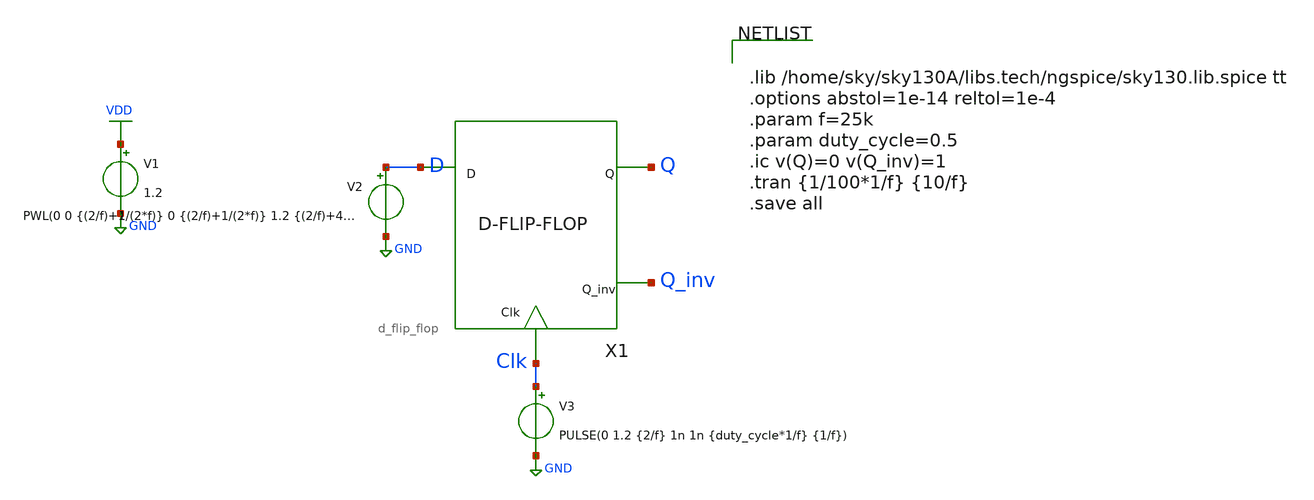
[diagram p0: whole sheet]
** sch_path: xschem/D_flip_flop/d_flip_flop_tb.sch
**.subckt d_flip_flop_tb
X1 D Q Q_inv Clk d_flip_flop
V1 VDD GND 1.2
V2 D GND PWL(0 0 {(2/f)+1/(2*f)} 0 {(2/f)+1/(2*f)} 1.2 {(2/f)+4/(2*f)} 1.2 {(2/f)+4/(2*f)} 0)
V3 Clk GND PULSE(0 1.2 {2/f} 1n 1n {duty_cycle*1/f} {1/f})
**** begin user architecture code


.lib /home/sky/sky130A/libs.tech/ngspice/sky130.lib.spice tt
.options abstol=1e-14 reltol=1e-4
.param f=25k
.param duty_cycle=0.5
.ic v(Q)=0 v(Q_inv)=1
.tran {1/100*1/f} {10/f}
.save all


**** end user architecture code
**.ends

* expanding   symbol:  D_flip_flop/d_flip_flop.sym # of pins=4
** sym_path: D_flip_flop/d_flip_flop.sym
** sch_path: D_flip_flop/d_flip_flop.sch
.subckt d_flip_flop D Q Q_inv Clk
*.ipin D
*.ipin Clk
*.opin Q_inv
*.opin Q
X1 net1 net2 inv
X2 net3 Q inv
X3 net2 net4 inv
X4 Q Q_inv inv
X5 D net1 Clk_inv Clk transmission_gate
X6 net1 net4 Clk Clk_inv transmission_gate
X7 net3 Q_inv Clk_inv Clk transmission_gate
X8 net2 net3 Clk Clk_inv transmission_gate
X9 Clk Clk_inv inv
.ends


* expanding   symbol:  inv/inv.sym # of pins=2
** sym_path: xschem/inv/inv.sym
** sch_path: xschem/inv/inv.sch
.subckt inv in out
*.ipin in
*.iopin out
XM1 out in GND GND sky130_fd_pr__nfet_01v8 L=0.18 W=0.5 nf=1 ad='int((nf+1)/2) * W/nf * 0.29' as='int((nf+2)/2) * W/nf * 0.29'
+ pd='2*int((nf+1)/2) * (W/nf + 0.29)' ps='2*int((nf+2)/2) * (W/nf + 0.29)' nrd='0.29 / W' nrs='0.29 / W'
+ sa=0 sb=0 sd=0 mult=1 m=1
XM2 out in VDD VDD sky130_fd_pr__pfet_01v8 L=0.18 W=1 nf=1 ad='int((nf+1)/2) * W/nf * 0.29' as='int((nf+2)/2) * W/nf * 0.29'
+ pd='2*int((nf+1)/2) * (W/nf + 0.29)' ps='2*int((nf+2)/2) * (W/nf + 0.29)' nrd='0.29 / W' nrs='0.29 / W'
+ sa=0 sb=0 sd=0 mult=1 m=1
.ends


* expanding   symbol:  transmission_gate/transmission_gate.sym # of pins=4
** sym_path: xschem/transmission_gate/transmission_gate.sym
** sch_path: xschem/transmission_gate/transmission_gate.sch
.subckt transmission_gate in out ctrl_ ctrl
*.iopin in
*.iopin out
*.ipin ctrl_
*.ipin ctrl
XM3 in ctrl out GND sky130_fd_pr__nfet_01v8 L=0.18 W=1 nf=1 ad='int((nf+1)/2) * W/nf * 0.29' as='int((nf+2)/2) * W/nf * 0.29'
+ pd='2*int((nf+1)/2) * (W/nf + 0.29)' ps='2*int((nf+2)/2) * (W/nf + 0.29)' nrd='0.29 / W' nrs='0.29 / W'
+ sa=0 sb=0 sd=0 mult=1 m=1
XM4 out ctrl_ in VDD sky130_fd_pr__pfet_01v8 L=0.18 W=1 nf=1 ad='int((nf+1)/2) * W/nf * 0.29' as='int((nf+2)/2) * W/nf * 0.29'
+ pd='2*int((nf+1)/2) * (W/nf + 0.29)' ps='2*int((nf+2)/2) * (W/nf + 0.29)' nrd='0.29 / W' nrs='0.29 / W'
+ sa=0 sb=0 sd=0 mult=1 m=1
.ends

.GLOBAL VDD
.GLOBAL GND
.end
